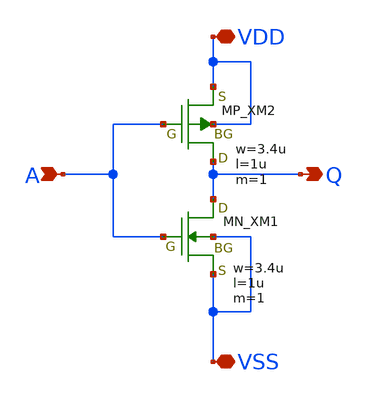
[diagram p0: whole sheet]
** sch_path: inverter/inverter_Shusuke_Isimaru.sch
**.subckt inverter_Shusuke_Isimaru VDD A Q VSS
*.iopin VDD
*.ipin A
*.opin Q
*.iopin VSS
XXM1 Q A VSS VSS NMOS w=3.4u l=1u nrd=0 nrs=0 m=1
XXM2 Q A VDD VDD PMOS w=3.4u l=1u nrd=0 nrs=0 m=1
**.ends
.end
